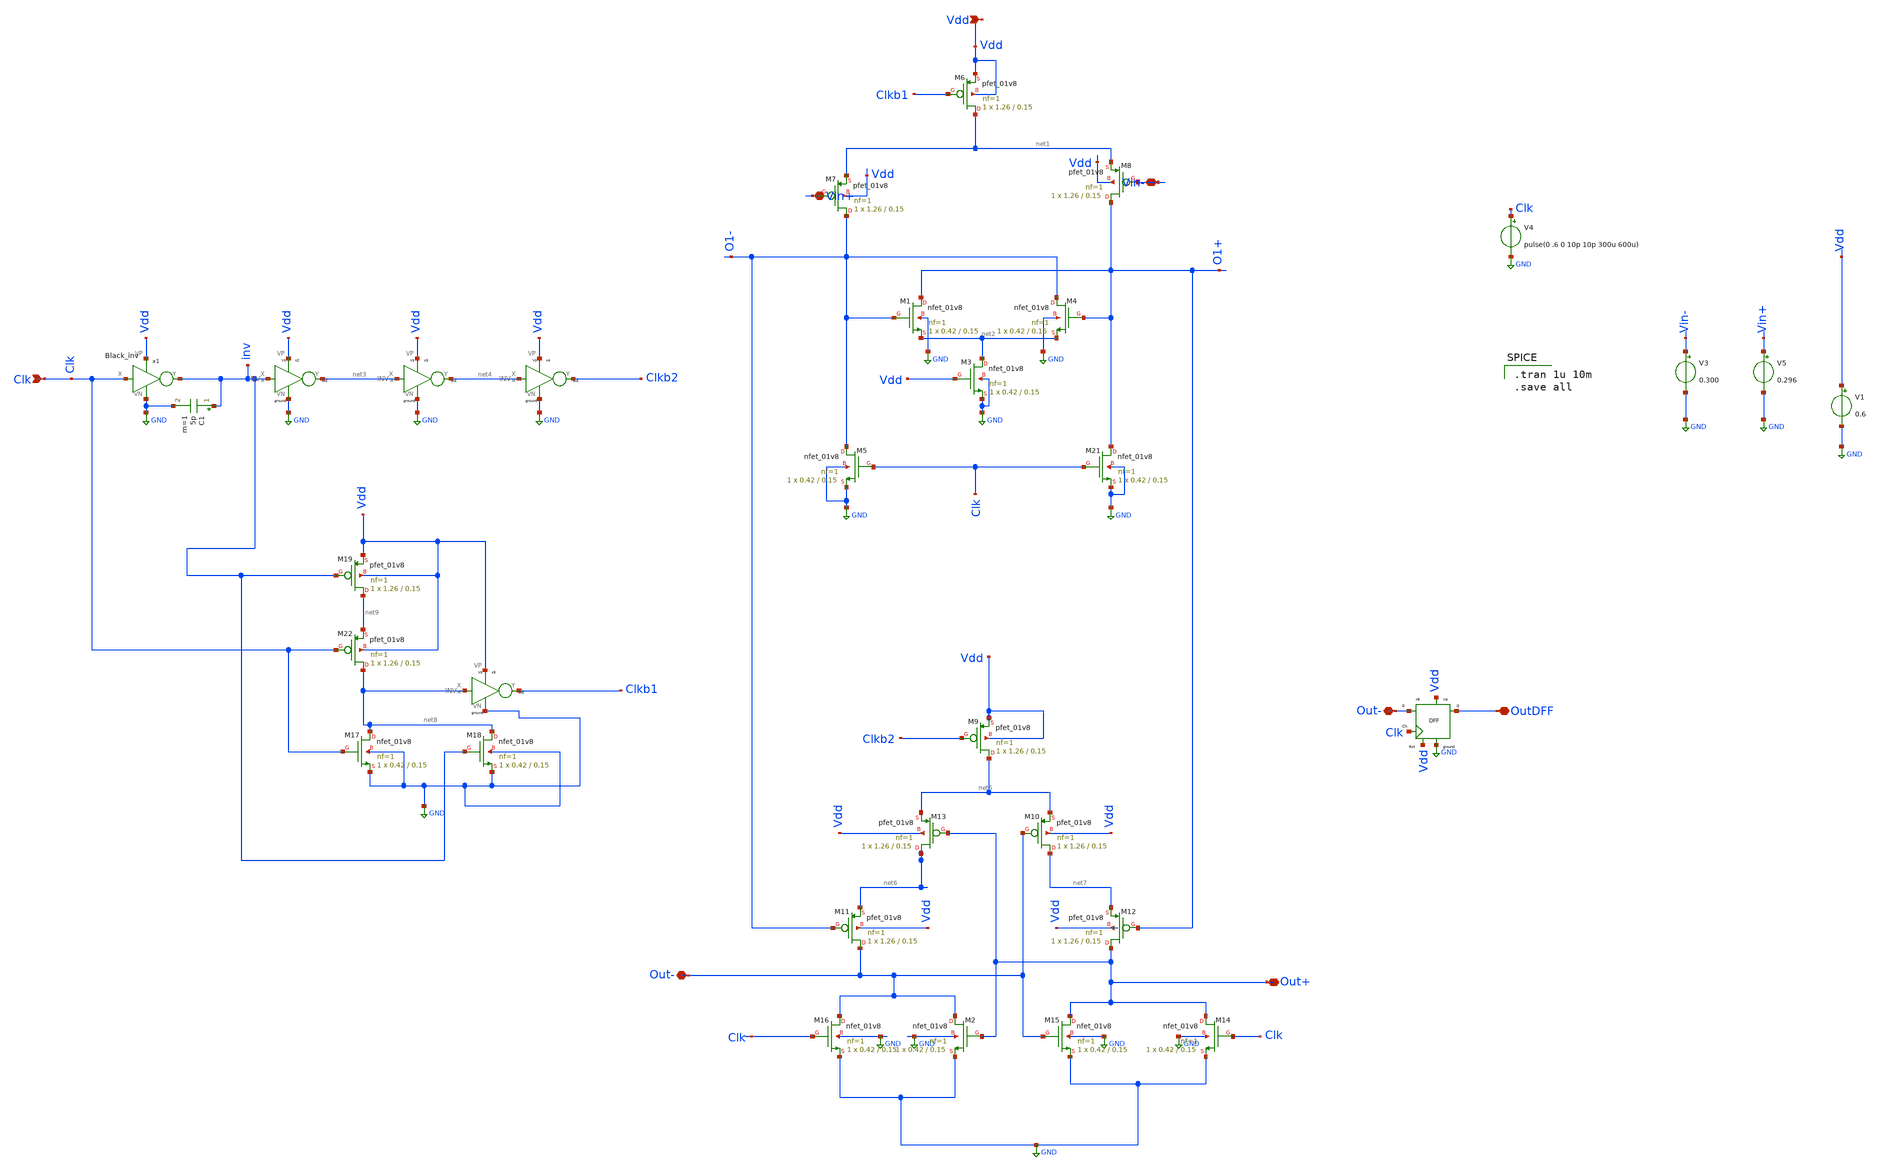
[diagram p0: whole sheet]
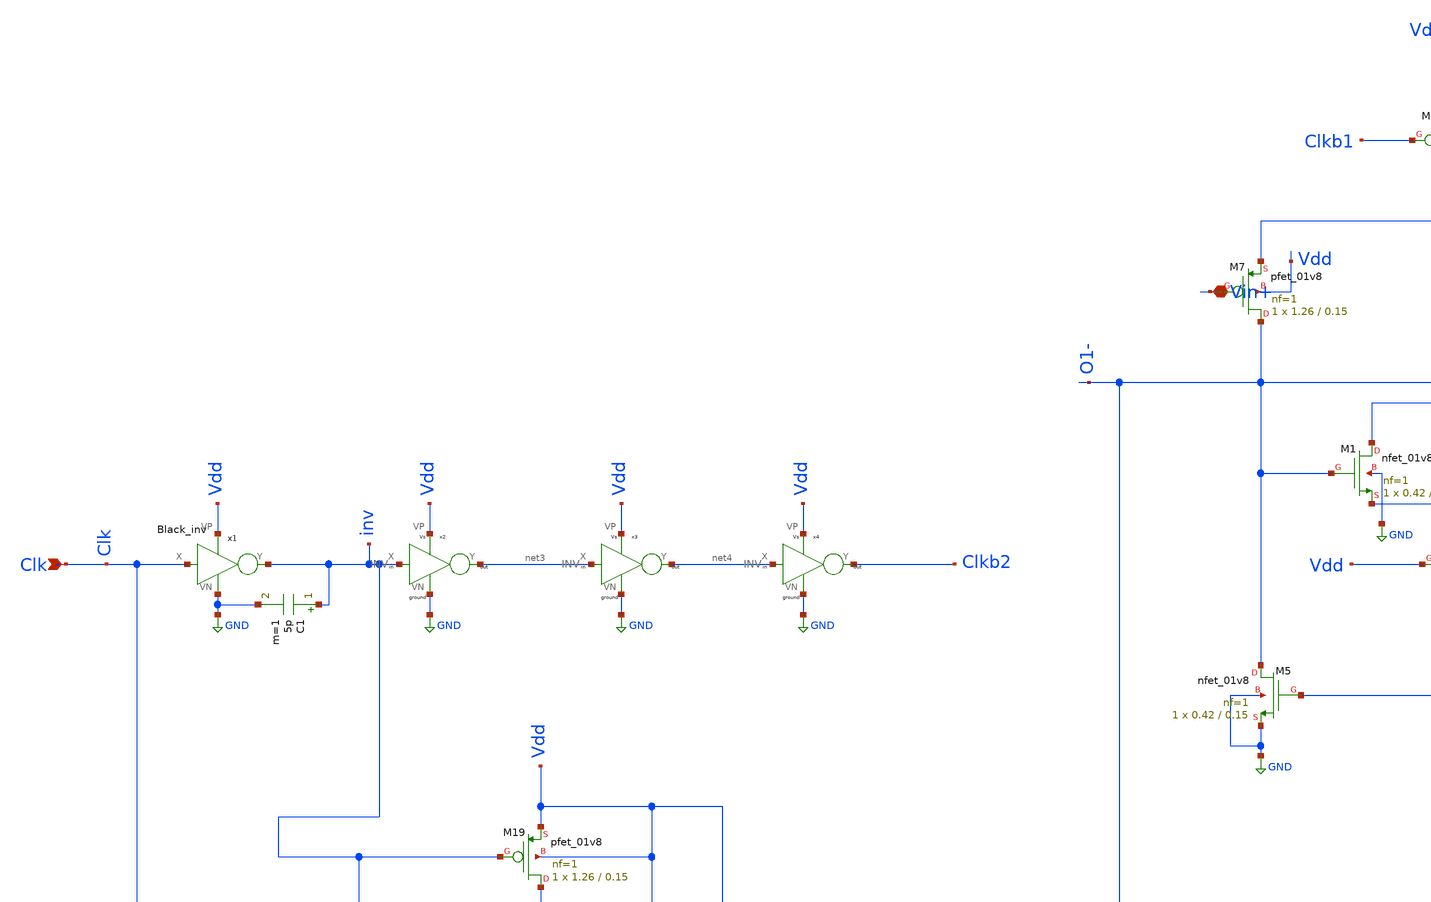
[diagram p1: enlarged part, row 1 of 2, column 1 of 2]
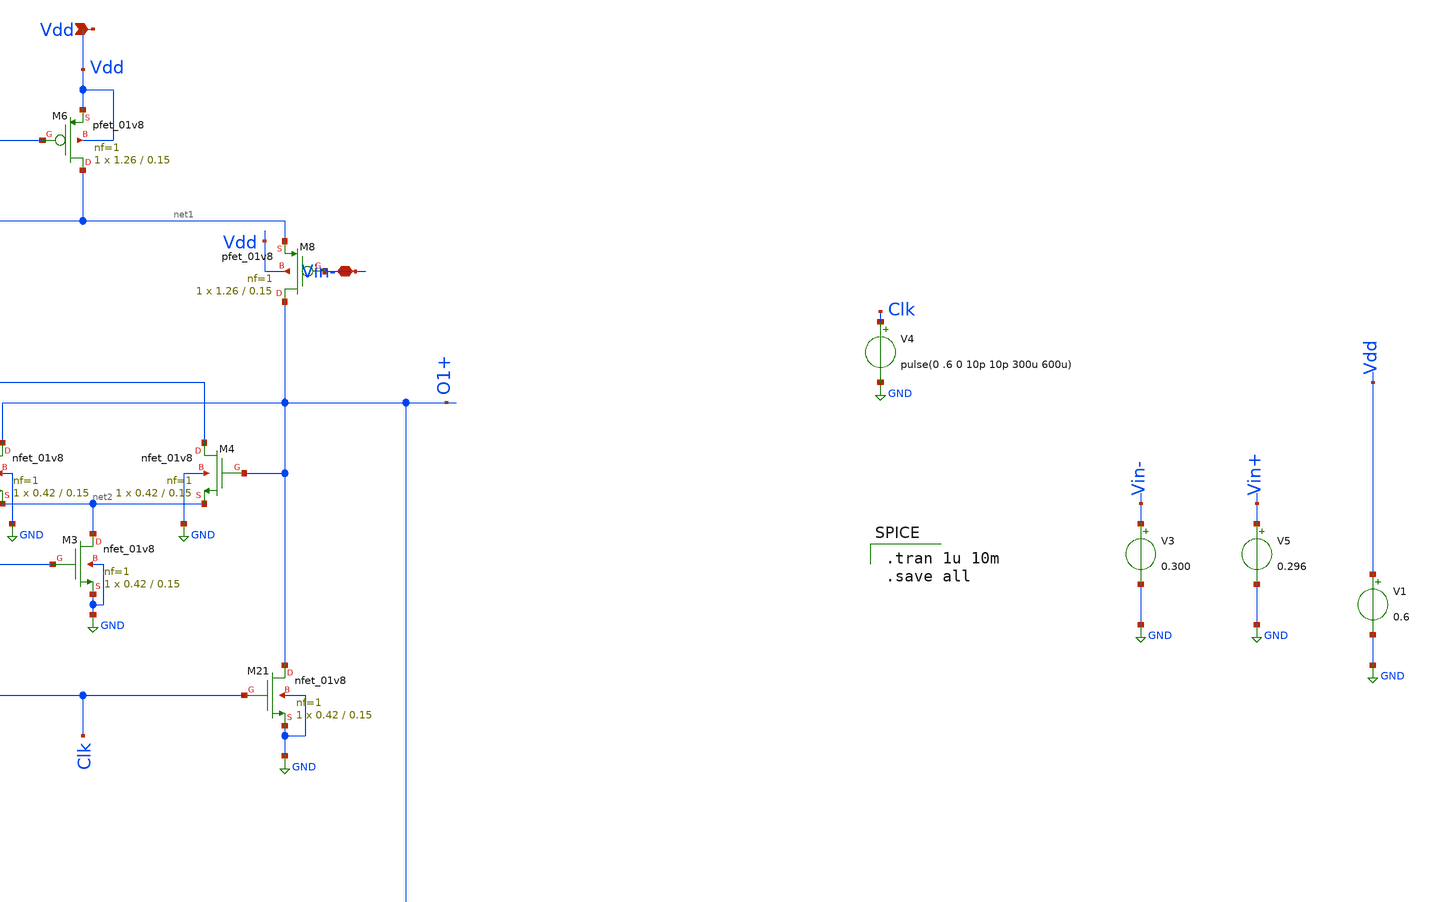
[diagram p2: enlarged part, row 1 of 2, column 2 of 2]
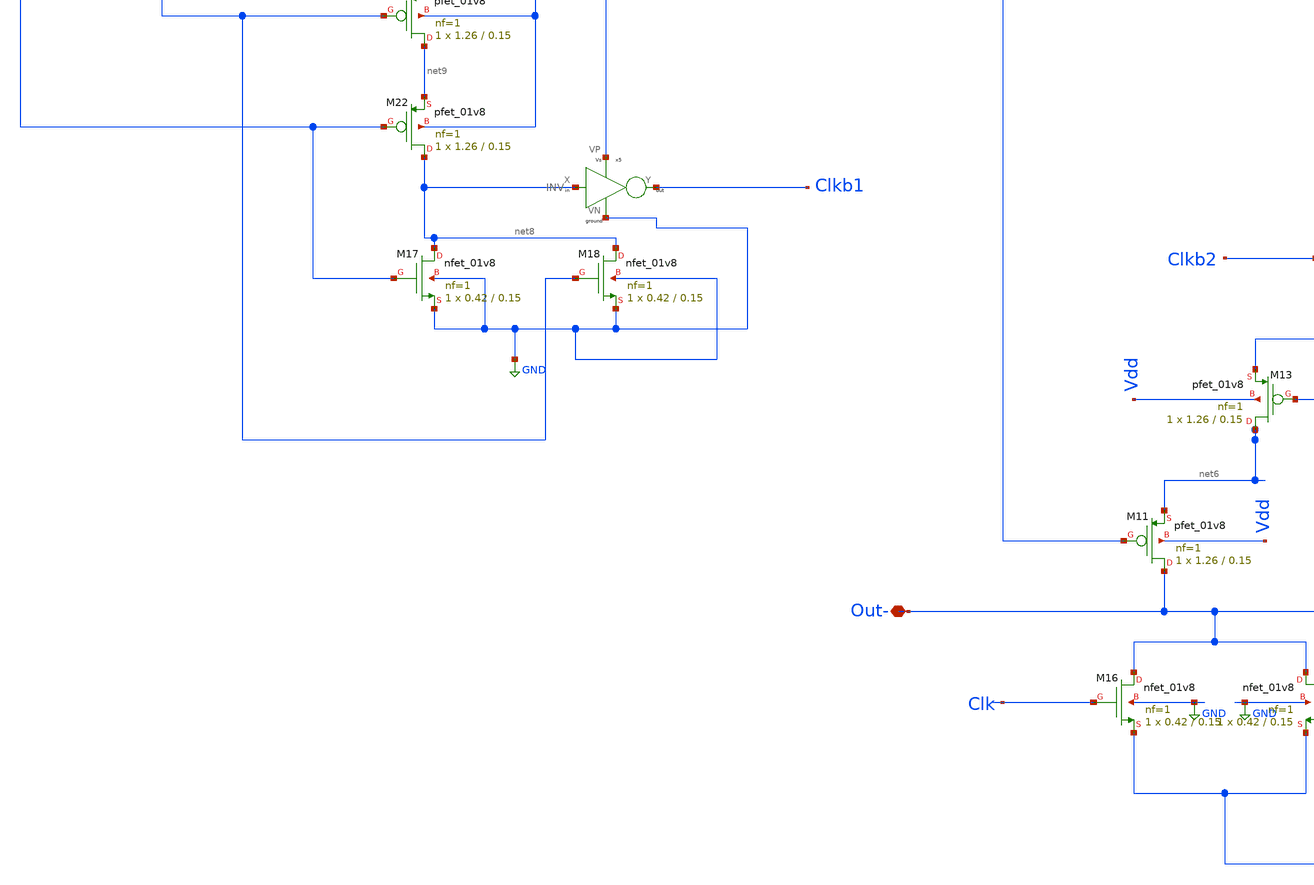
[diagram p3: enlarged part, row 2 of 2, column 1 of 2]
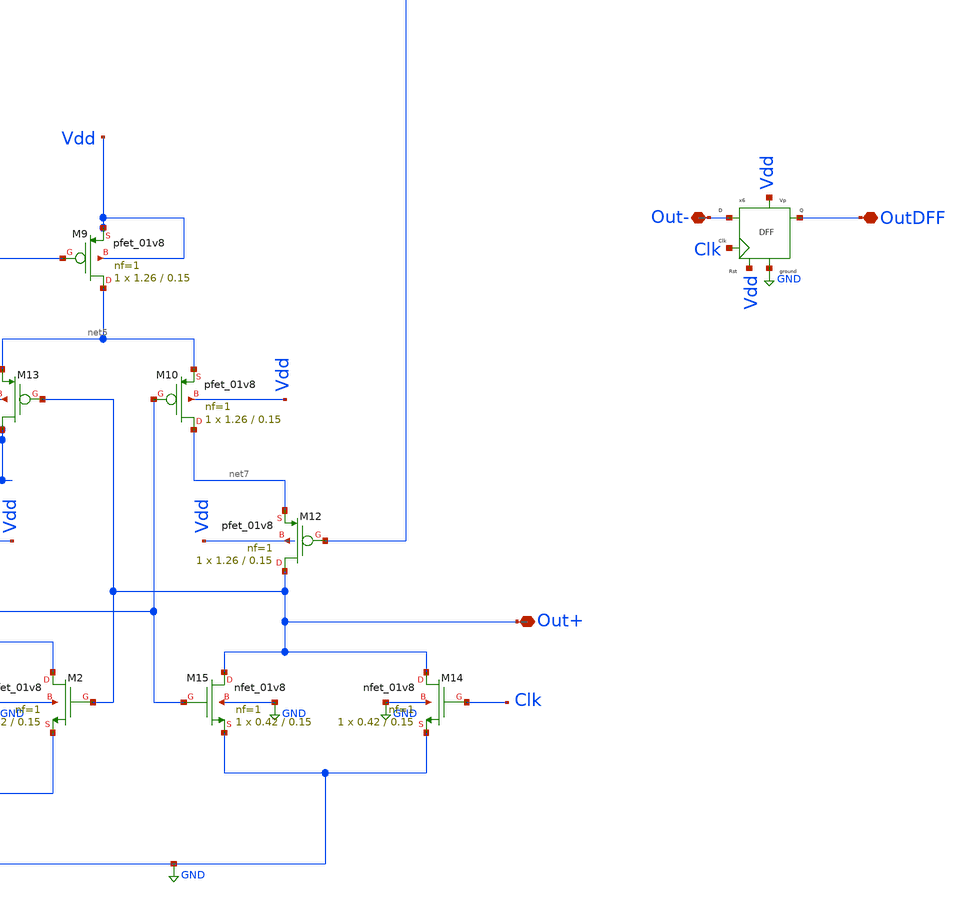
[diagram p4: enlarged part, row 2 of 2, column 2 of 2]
** sch_path: Blocks/comparator_150nm/Com_test_150_clkgen (kaja).sch
**.subckt Com_test_150_clkgen (kaja) Vin+ Vin- Out+ Out- Vdd Clk Out- OutDFF
*.iopin Vin+
*.iopin Vin-
*.iopin Out+
*.iopin Out-
*.ipin Vdd
*.ipin Clk
*.iopin Out-
*.iopin OutDFF
XM6 net1 Clkb1 Vdd Vdd sky130_fd_pr__pfet_01v8 L=0.15 W=1.26 nf=1 ad='int((nf+1)/2) * W/nf * 0.29' as='int((nf+2)/2) * W/nf * 0.29'
+ pd='2*int((nf+1)/2) * (W/nf + 0.29)' ps='2*int((nf+2)/2) * (W/nf + 0.29)' nrd='0.29 / W' nrs='0.29 / W'
+ sa=0 sb=0 sd=0 mult=1 m=1
XM7 O1- Vin+ net1 Vdd sky130_fd_pr__pfet_01v8 L=0.15 W=1.26 nf=1 ad='int((nf+1)/2) * W/nf * 0.29' as='int((nf+2)/2) * W/nf * 0.29'
+ pd='2*int((nf+1)/2) * (W/nf + 0.29)' ps='2*int((nf+2)/2) * (W/nf + 0.29)' nrd='0.29 / W' nrs='0.29 / W'
+ sa=0 sb=0 sd=0 mult=1 m=1
XM8 O1+ Vin- net1 Vdd sky130_fd_pr__pfet_01v8 L=0.15 W=1.26 nf=1 ad='int((nf+1)/2) * W/nf * 0.29' as='int((nf+2)/2) * W/nf * 0.29'
+ pd='2*int((nf+1)/2) * (W/nf + 0.29)' ps='2*int((nf+2)/2) * (W/nf + 0.29)' nrd='0.29 / W' nrs='0.29 / W'
+ sa=0 sb=0 sd=0 mult=1 m=1
XM9 net5 Clkb2 Vdd Vdd sky130_fd_pr__pfet_01v8 L=0.15 W=1.26 nf=1 ad='int((nf+1)/2) * W/nf * 0.29' as='int((nf+2)/2) * W/nf * 0.29'
+ pd='2*int((nf+1)/2) * (W/nf + 0.29)' ps='2*int((nf+2)/2) * (W/nf + 0.29)' nrd='0.29 / W' nrs='0.29 / W'
+ sa=0 sb=0 sd=0 mult=1 m=1
XM10 net7 Out- net5 Vdd sky130_fd_pr__pfet_01v8 L=0.15 W=1.26 nf=1 ad='int((nf+1)/2) * W/nf * 0.29' as='int((nf+2)/2) * W/nf * 0.29'
+ pd='2*int((nf+1)/2) * (W/nf + 0.29)' ps='2*int((nf+2)/2) * (W/nf + 0.29)' nrd='0.29 / W' nrs='0.29 / W'
+ sa=0 sb=0 sd=0 mult=1 m=1
XM11 Out- O1- net6 Vdd sky130_fd_pr__pfet_01v8 L=0.15 W=1.26 nf=1 ad='int((nf+1)/2) * W/nf * 0.29' as='int((nf+2)/2) * W/nf * 0.29'
+ pd='2*int((nf+1)/2) * (W/nf + 0.29)' ps='2*int((nf+2)/2) * (W/nf + 0.29)' nrd='0.29 / W' nrs='0.29 / W'
+ sa=0 sb=0 sd=0 mult=1 m=1
XM12 Out+ O1+ net7 Vdd sky130_fd_pr__pfet_01v8 L=0.15 W=1.26 nf=1 ad='int((nf+1)/2) * W/nf * 0.29' as='int((nf+2)/2) * W/nf * 0.29'
+ pd='2*int((nf+1)/2) * (W/nf + 0.29)' ps='2*int((nf+2)/2) * (W/nf + 0.29)' nrd='0.29 / W' nrs='0.29 / W'
+ sa=0 sb=0 sd=0 mult=1 m=1
XM13 net6 Out+ net5 Vdd sky130_fd_pr__pfet_01v8 L=0.15 W=1.26 nf=1 ad='int((nf+1)/2) * W/nf * 0.29' as='int((nf+2)/2) * W/nf * 0.29'
+ pd='2*int((nf+1)/2) * (W/nf + 0.29)' ps='2*int((nf+2)/2) * (W/nf + 0.29)' nrd='0.29 / W' nrs='0.29 / W'
+ sa=0 sb=0 sd=0 mult=1 m=1
XM1 O1+ O1- net2 GND sky130_fd_pr__nfet_01v8 L=0.15 W=0.42 nf=1 ad='int((nf+1)/2) * W/nf * 0.29' as='int((nf+2)/2) * W/nf * 0.29'
+ pd='2*int((nf+1)/2) * (W/nf + 0.29)' ps='2*int((nf+2)/2) * (W/nf + 0.29)' nrd='0.29 / W' nrs='0.29 / W'
+ sa=0 sb=0 sd=0 mult=1 m=1
XM3 net2 Vdd GND GND sky130_fd_pr__nfet_01v8 L=0.15 W=0.42 nf=1 ad='int((nf+1)/2) * W/nf * 0.29' as='int((nf+2)/2) * W/nf * 0.29'
+ pd='2*int((nf+1)/2) * (W/nf + 0.29)' ps='2*int((nf+2)/2) * (W/nf + 0.29)' nrd='0.29 / W' nrs='0.29 / W'
+ sa=0 sb=0 sd=0 mult=1 m=1
XM4 O1- O1+ net2 GND sky130_fd_pr__nfet_01v8 L=0.15 W=0.42 nf=1 ad='int((nf+1)/2) * W/nf * 0.29' as='int((nf+2)/2) * W/nf * 0.29'
+ pd='2*int((nf+1)/2) * (W/nf + 0.29)' ps='2*int((nf+2)/2) * (W/nf + 0.29)' nrd='0.29 / W' nrs='0.29 / W'
+ sa=0 sb=0 sd=0 mult=1 m=1
XM5 O1- Clk GND GND sky130_fd_pr__nfet_01v8 L=0.15 W=0.42 nf=1 ad='int((nf+1)/2) * W/nf * 0.29' as='int((nf+2)/2) * W/nf * 0.29'
+ pd='2*int((nf+1)/2) * (W/nf + 0.29)' ps='2*int((nf+2)/2) * (W/nf + 0.29)' nrd='0.29 / W' nrs='0.29 / W'
+ sa=0 sb=0 sd=0 mult=1 m=1
XM21 O1+ Clk GND GND sky130_fd_pr__nfet_01v8 L=0.15 W=0.42 nf=1 ad='int((nf+1)/2) * W/nf * 0.29' as='int((nf+2)/2) * W/nf * 0.29'
+ pd='2*int((nf+1)/2) * (W/nf + 0.29)' ps='2*int((nf+2)/2) * (W/nf + 0.29)' nrd='0.29 / W' nrs='0.29 / W'
+ sa=0 sb=0 sd=0 mult=1 m=1
XM2 Out- Out+ GND GND sky130_fd_pr__nfet_01v8 L=0.15 W=0.42 nf=1 ad='int((nf+1)/2) * W/nf * 0.29' as='int((nf+2)/2) * W/nf * 0.29'
+ pd='2*int((nf+1)/2) * (W/nf + 0.29)' ps='2*int((nf+2)/2) * (W/nf + 0.29)' nrd='0.29 / W' nrs='0.29 / W'
+ sa=0 sb=0 sd=0 mult=1 m=1
XM14 Out+ Clk GND GND sky130_fd_pr__nfet_01v8 L=0.15 W=0.42 nf=1 ad='int((nf+1)/2) * W/nf * 0.29' as='int((nf+2)/2) * W/nf * 0.29'
+ pd='2*int((nf+1)/2) * (W/nf + 0.29)' ps='2*int((nf+2)/2) * (W/nf + 0.29)' nrd='0.29 / W' nrs='0.29 / W'
+ sa=0 sb=0 sd=0 mult=1 m=1
XM15 Out+ Out- GND GND sky130_fd_pr__nfet_01v8 L=0.15 W=0.42 nf=1 ad='int((nf+1)/2) * W/nf * 0.29' as='int((nf+2)/2) * W/nf * 0.29'
+ pd='2*int((nf+1)/2) * (W/nf + 0.29)' ps='2*int((nf+2)/2) * (W/nf + 0.29)' nrd='0.29 / W' nrs='0.29 / W'
+ sa=0 sb=0 sd=0 mult=1 m=1
XM16 Out- Clk GND GND sky130_fd_pr__nfet_01v8 L=0.15 W=0.42 nf=1 ad='int((nf+1)/2) * W/nf * 0.29' as='int((nf+2)/2) * W/nf * 0.29'
+ pd='2*int((nf+1)/2) * (W/nf + 0.29)' ps='2*int((nf+2)/2) * (W/nf + 0.29)' nrd='0.29 / W' nrs='0.29 / W'
+ sa=0 sb=0 sd=0 mult=1 m=1
XM17 net8 Clk GND GND sky130_fd_pr__nfet_01v8 L=0.15 W=0.42 nf=1 ad='int((nf+1)/2) * W/nf * 0.29' as='int((nf+2)/2) * W/nf * 0.29'
+ pd='2*int((nf+1)/2) * (W/nf + 0.29)' ps='2*int((nf+2)/2) * (W/nf + 0.29)' nrd='0.29 / W' nrs='0.29 / W'
+ sa=0 sb=0 sd=0 mult=1 m=1
XM18 net8 inv GND GND sky130_fd_pr__nfet_01v8 L=0.15 W=0.42 nf=1 ad='int((nf+1)/2) * W/nf * 0.29' as='int((nf+2)/2) * W/nf * 0.29'
+ pd='2*int((nf+1)/2) * (W/nf + 0.29)' ps='2*int((nf+2)/2) * (W/nf + 0.29)' nrd='0.29 / W' nrs='0.29 / W'
+ sa=0 sb=0 sd=0 mult=1 m=1
XM19 net9 inv Vdd Vdd sky130_fd_pr__pfet_01v8 L=0.15 W=1.26 nf=1 ad='int((nf+1)/2) * W/nf * 0.29' as='int((nf+2)/2) * W/nf * 0.29'
+ pd='2*int((nf+1)/2) * (W/nf + 0.29)' ps='2*int((nf+2)/2) * (W/nf + 0.29)' nrd='0.29 / W' nrs='0.29 / W'
+ sa=0 sb=0 sd=0 mult=1 m=1
XM22 net8 Clk net9 Vdd sky130_fd_pr__pfet_01v8 L=0.15 W=1.26 nf=1 ad='int((nf+1)/2) * W/nf * 0.29' as='int((nf+2)/2) * W/nf * 0.29'
+ pd='2*int((nf+1)/2) * (W/nf + 0.29)' ps='2*int((nf+2)/2) * (W/nf + 0.29)' nrd='0.29 / W' nrs='0.29 / W'
+ sa=0 sb=0 sd=0 mult=1 m=1
V3 Vin- GND 0.300
V5 Vin+ GND 0.296
V1 Vdd GND 0.6
V4 Clk GND pulse(0 .6 0 10p 10p 300u 600u)
C1 inv GND 5p m=1
x1 Clk inv Vdd GND black_inv
x2 inv net3 Vdd GND INV
x3 net3 net4 Vdd GND INV
x4 net4 Clkb2 Vdd GND INV
x5 net8 Clkb1 Vdd GND INV
x6 Out- Clk Vdd GND Vdd OutDFF DFF
**** begin user architecture code

** opencircuitdesign pdks install
.lib $::SKYWATER_MODELS/sky130.lib.spice tt



.tran 1u 10m
.save all

**** end user architecture code
**.ends

* expanding   symbol:  pico_chipathon/component/black_inv_1/black_inv.sym # of pins=4
** sym_path: component/black_inv_1/black_inv.sym
** sch_path: component/black_inv_1/black_inv.sch
.subckt black_inv X Y VP VN
*.ipin X
*.opin Y
*.iopin VN
*.iopin VP
XM8 Y X VP VP sky130_fd_pr__pfet_01v8 L=.18 W=1.59 nf=1 ad='int((nf+1)/2) * W/nf * 0.29' as='int((nf+2)/2) * W/nf * 0.29'
+ pd='2*int((nf+1)/2) * (W/nf + 0.29)' ps='2*int((nf+2)/2) * (W/nf + 0.29)' nrd='0.29 / W' nrs='0.29 / W'
+ sa=0 sb=0 sd=0 mult=1 m=1
XM4 Y X VN VN sky130_fd_pr__nfet_01v8 L=0.18 W=0.502 nf=1 ad='int((nf+1)/2) * W/nf * 0.29' as='int((nf+2)/2) * W/nf * 0.29'
+ pd='2*int((nf+1)/2) * (W/nf + 0.29)' ps='2*int((nf+2)/2) * (W/nf + 0.29)' nrd='0.29 / W' nrs='0.29 / W'
+ sa=0 sb=0 sd=0 mult=1 m=1
.ends


* expanding   symbol:  pico_chipathon/component/INV/INV.sym # of pins=4
** sym_path: component/INV/INV.sym
** sch_path: component/INV/INV.sch
.subckt INV X Y VP VN
*.ipin X
*.opin Y
*.iopin VN
*.iopin VP
XM1 Y X VN VN sky130_fd_pr__nfet_01v8 L=0.15 W=0.42 nf=1 ad='int((nf+1)/2) * W/nf * 0.29' as='int((nf+2)/2) * W/nf * 0.29'
+ pd='2*int((nf+1)/2) * (W/nf + 0.29)' ps='2*int((nf+2)/2) * (W/nf + 0.29)' nrd='0.29 / W' nrs='0.29 / W'
+ sa=0 sb=0 sd=0 mult=1 m=1
XM2 Y X VP VP sky130_fd_pr__pfet_01v8 L=0.15 W=1.26 nf=1 ad='int((nf+1)/2) * W/nf * 0.29' as='int((nf+2)/2) * W/nf * 0.29'
+ pd='2*int((nf+1)/2) * (W/nf + 0.29)' ps='2*int((nf+2)/2) * (W/nf + 0.29)' nrd='0.29 / W' nrs='0.29 / W'
+ sa=0 sb=0 sd=0 mult=1 m=1
.ends


* expanding   symbol:  pico_chipathon/component/FlipFlops/DFF.sym # of pins=6
** sym_path: component/FlipFlops/DFF.sym
** sch_path: component/FlipFlops/DFF.sch
.subckt DFF D Clk RST VN VP Q
*.opin Q
*.iopin VN
*.iopin VP
*.ipin Clk
*.ipin D
*.ipin RST
x1 net2 net5 net4 VP VN NAND
x7 net4 Clk RST VP VN net2 NAND3
x3 Q net1 RST VP VN net3 NAND3
x4 net2 Clk net5 VP VN net1 NAND3
x5 net1 D RST VP VN net5 NAND3
x6 net3 net2 Q VP VN NAND
.ends


* expanding   symbol:  component/NAND2/NAND.sym # of pins=5
** sym_path: component/NAND2/NAND.sym
** sch_path: component/NAND2/NAND.sch
.subckt NAND B A Y VP VN
*.iopin VP
*.ipin A
*.ipin B
*.opin Y
*.iopin VN
XM1 Y A VP VP sky130_fd_pr__pfet_01v8 L=0.15 W=1.26 nf=1 ad='int((nf+1)/2) * W/nf * 0.29' as='int((nf+2)/2) * W/nf * 0.29'
+ pd='2*int((nf+1)/2) * (W/nf + 0.29)' ps='2*int((nf+2)/2) * (W/nf + 0.29)' nrd='0.29 / W' nrs='0.29 / W'
+ sa=0 sb=0 sd=0 mult=1 m=1
XM2 Y B VP VP sky130_fd_pr__pfet_01v8 L=0.15 W=1.26 nf=1 ad='int((nf+1)/2) * W/nf * 0.29' as='int((nf+2)/2) * W/nf * 0.29'
+ pd='2*int((nf+1)/2) * (W/nf + 0.29)' ps='2*int((nf+2)/2) * (W/nf + 0.29)' nrd='0.29 / W' nrs='0.29 / W'
+ sa=0 sb=0 sd=0 mult=1 m=1
XM3 Y A net1 net1 sky130_fd_pr__nfet_01v8 L=0.15 W=0.84 nf=1 ad='int((nf+1)/2) * W/nf * 0.29' as='int((nf+2)/2) * W/nf * 0.29'
+ pd='2*int((nf+1)/2) * (W/nf + 0.29)' ps='2*int((nf+2)/2) * (W/nf + 0.29)' nrd='0.29 / W' nrs='0.29 / W'
+ sa=0 sb=0 sd=0 mult=1 m=1
XM4 net1 B VN VN sky130_fd_pr__nfet_01v8 L=0.15 W=0.84 nf=1 ad='int((nf+1)/2) * W/nf * 0.29' as='int((nf+2)/2) * W/nf * 0.29'
+ pd='2*int((nf+1)/2) * (W/nf + 0.29)' ps='2*int((nf+2)/2) * (W/nf + 0.29)' nrd='0.29 / W' nrs='0.29 / W'
+ sa=0 sb=0 sd=0 mult=1 m=1
.ends


* expanding   symbol:  component/NAND3/NAND3.sym # of pins=6
** sym_path: component/NAND3/NAND3.sym
** sch_path: component/NAND3/NAND3.sch
.subckt NAND3 A B C VP VN Y
*.iopin VP
*.iopin VN
*.ipin A
*.ipin B
*.ipin C
*.opin Y
XM1 Y A net1 VN sky130_fd_pr__nfet_01v8 L=0.15 W=1.26 nf=1 ad='int((nf+1)/2) * W/nf * 0.29' as='int((nf+2)/2) * W/nf * 0.29'
+ pd='2*int((nf+1)/2) * (W/nf + 0.29)' ps='2*int((nf+2)/2) * (W/nf + 0.29)' nrd='0.29 / W' nrs='0.29 / W'
+ sa=0 sb=0 sd=0 mult=1 m=1
XM2 net1 B net2 VN sky130_fd_pr__nfet_01v8 L=0.15 W=1.26 nf=1 ad='int((nf+1)/2) * W/nf * 0.29' as='int((nf+2)/2) * W/nf * 0.29'
+ pd='2*int((nf+1)/2) * (W/nf + 0.29)' ps='2*int((nf+2)/2) * (W/nf + 0.29)' nrd='0.29 / W' nrs='0.29 / W'
+ sa=0 sb=0 sd=0 mult=1 m=1
XM3 net2 C VN VN sky130_fd_pr__nfet_01v8 L=0.15 W=1.26 nf=1 ad='int((nf+1)/2) * W/nf * 0.29' as='int((nf+2)/2) * W/nf * 0.29'
+ pd='2*int((nf+1)/2) * (W/nf + 0.29)' ps='2*int((nf+2)/2) * (W/nf + 0.29)' nrd='0.29 / W' nrs='0.29 / W'
+ sa=0 sb=0 sd=0 mult=1 m=1
XM4 Y A VP VP sky130_fd_pr__pfet_01v8 L=0.15 W=1.26 nf=1 ad='int((nf+1)/2) * W/nf * 0.29' as='int((nf+2)/2) * W/nf * 0.29'
+ pd='2*int((nf+1)/2) * (W/nf + 0.29)' ps='2*int((nf+2)/2) * (W/nf + 0.29)' nrd='0.29 / W' nrs='0.29 / W'
+ sa=0 sb=0 sd=0 mult=1 m=1
XM5 Y B VP VP sky130_fd_pr__pfet_01v8 L=0.15 W=1.26 nf=1 ad='int((nf+1)/2) * W/nf * 0.29' as='int((nf+2)/2) * W/nf * 0.29'
+ pd='2*int((nf+1)/2) * (W/nf + 0.29)' ps='2*int((nf+2)/2) * (W/nf + 0.29)' nrd='0.29 / W' nrs='0.29 / W'
+ sa=0 sb=0 sd=0 mult=1 m=1
XM6 Y C VP VP sky130_fd_pr__pfet_01v8 L=0.15 W=1.26 nf=1 ad='int((nf+1)/2) * W/nf * 0.29' as='int((nf+2)/2) * W/nf * 0.29'
+ pd='2*int((nf+1)/2) * (W/nf + 0.29)' ps='2*int((nf+2)/2) * (W/nf + 0.29)' nrd='0.29 / W' nrs='0.29 / W'
+ sa=0 sb=0 sd=0 mult=1 m=1
.ends

.GLOBAL GND
.end
